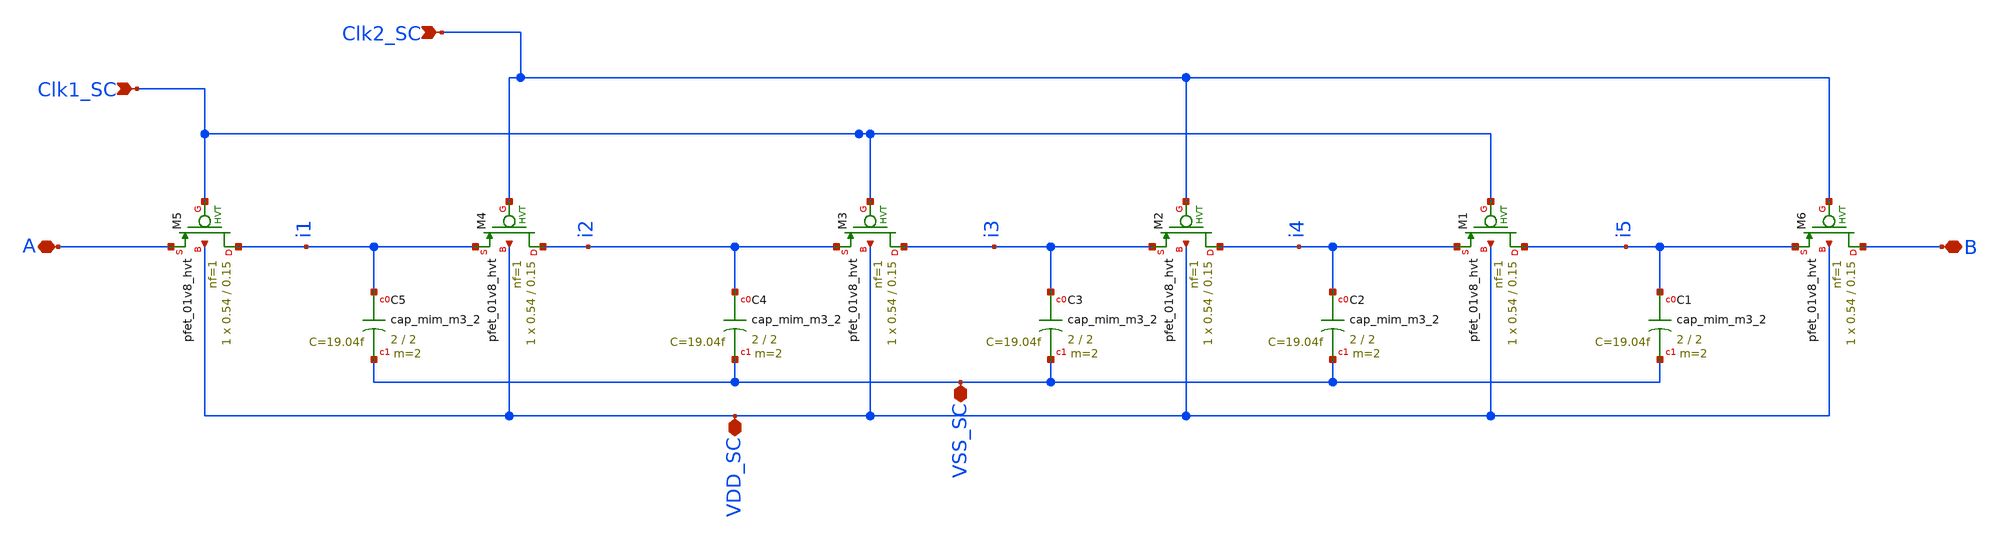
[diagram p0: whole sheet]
** sch_path: SC_FB.sch
**.subckt SC_FB A Clk1_SC Clk2_SC VSS_SC B VDD_SC
*.iopin A
*.ipin Clk1_SC
*.ipin Clk2_SC
*.iopin VSS_SC
*.iopin B
*.iopin VDD_SC
XC1 i5 VSS_SC sky130_fd_pr__cap_mim_m3_2 W=2 L=2 MF=2 m=2
XC2 i4 VSS_SC sky130_fd_pr__cap_mim_m3_2 W=2 L=2 MF=2 m=2
XC3 i3 VSS_SC sky130_fd_pr__cap_mim_m3_2 W=2 L=2 MF=2 m=2
XC4 i2 VSS_SC sky130_fd_pr__cap_mim_m3_2 W=2 L=2 MF=2 m=2
XM1 i5 Clk1_SC i4 VDD_SC sky130_fd_pr__pfet_01v8_hvt L=0.15 W=0.54 nf=1 ad='int((nf+1)/2) * W/nf * 0.29'
+ as='int((nf+2)/2) * W/nf * 0.29' pd='2*int((nf+1)/2) * (W/nf + 0.29)' ps='2*int((nf+2)/2) * (W/nf + 0.29)'
+ nrd='0.29 / W' nrs='0.29 / W' sa=0 sb=0 sd=0 mult=1 m=1
XM2 i4 Clk2_SC i3 VDD_SC sky130_fd_pr__pfet_01v8_hvt L=0.15 W=0.54 nf=1 ad='int((nf+1)/2) * W/nf * 0.29'
+ as='int((nf+2)/2) * W/nf * 0.29' pd='2*int((nf+1)/2) * (W/nf + 0.29)' ps='2*int((nf+2)/2) * (W/nf + 0.29)'
+ nrd='0.29 / W' nrs='0.29 / W' sa=0 sb=0 sd=0 mult=1 m=1
XM3 i3 Clk1_SC i2 VDD_SC sky130_fd_pr__pfet_01v8_hvt L=0.15 W=0.54 nf=1 ad='int((nf+1)/2) * W/nf * 0.29'
+ as='int((nf+2)/2) * W/nf * 0.29' pd='2*int((nf+1)/2) * (W/nf + 0.29)' ps='2*int((nf+2)/2) * (W/nf + 0.29)'
+ nrd='0.29 / W' nrs='0.29 / W' sa=0 sb=0 sd=0 mult=1 m=1
XM4 i2 Clk2_SC i1 VDD_SC sky130_fd_pr__pfet_01v8_hvt L=0.15 W=0.54 nf=1 ad='int((nf+1)/2) * W/nf * 0.29'
+ as='int((nf+2)/2) * W/nf * 0.29' pd='2*int((nf+1)/2) * (W/nf + 0.29)' ps='2*int((nf+2)/2) * (W/nf + 0.29)'
+ nrd='0.29 / W' nrs='0.29 / W' sa=0 sb=0 sd=0 mult=1 m=1
XM5 i1 Clk1_SC A VDD_SC sky130_fd_pr__pfet_01v8_hvt L=0.15 W=0.54 nf=1 ad='int((nf+1)/2) * W/nf * 0.29'
+ as='int((nf+2)/2) * W/nf * 0.29' pd='2*int((nf+1)/2) * (W/nf + 0.29)' ps='2*int((nf+2)/2) * (W/nf + 0.29)'
+ nrd='0.29 / W' nrs='0.29 / W' sa=0 sb=0 sd=0 mult=1 m=1
XM6 B Clk2_SC i5 VDD_SC sky130_fd_pr__pfet_01v8_hvt L=0.15 W=0.54 nf=1 ad='int((nf+1)/2) * W/nf * 0.29'
+ as='int((nf+2)/2) * W/nf * 0.29' pd='2*int((nf+1)/2) * (W/nf + 0.29)' ps='2*int((nf+2)/2) * (W/nf + 0.29)'
+ nrd='0.29 / W' nrs='0.29 / W' sa=0 sb=0 sd=0 mult=1 m=1
XC5 i1 VSS_SC sky130_fd_pr__cap_mim_m3_2 W=2 L=2 MF=2 m=2
**.ends
.end
